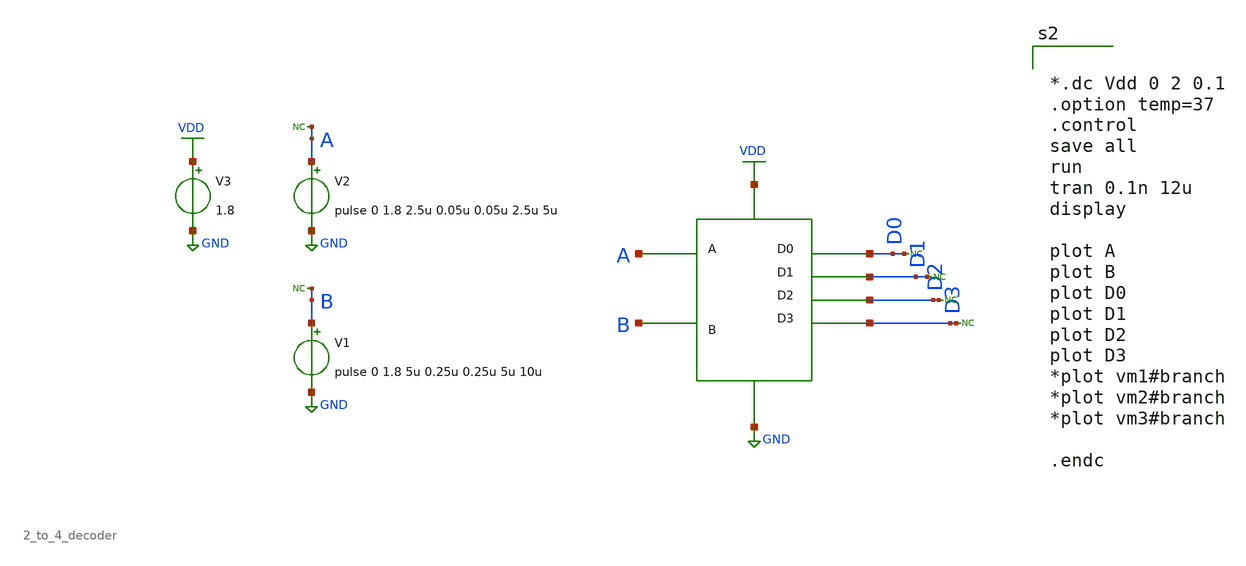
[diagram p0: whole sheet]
** sch_path: xschem/ip_block/logic_gate/tb_2_to_4_decoder.sch
**.subckt tb_2_to_4_decoder
V1 B GND pulse 0 1.8 5u 0.25u 0.25u 5u 10u
* noconn B
V2 A GND pulse 0 1.8 2.5u 0.05u 0.05u 2.5u 5u
* noconn A
V3 VDD GND 1.8
X1 A GND VDD B D0 D1 D2 D3 2_to_4_decoder
* noconn D0
* noconn D1
* noconn D2
* noconn D3
**** begin user architecture code

** opencircuitdesign pdks install
.lib $::SKYWATER_MODELS/sky130.lib.spice tt




*.dc Vdd 0 2 0.1
.option temp=37
.control
save all
run
tran 0.1n 12u
display

plot A
plot B
plot D0
plot D1
plot D2
plot D3
*plot vm1#branch
*plot vm2#branch
*plot vm3#branch

.endc


**** end user architecture code
**.ends
.GLOBAL GND
.GLOBAL VDD
.end
